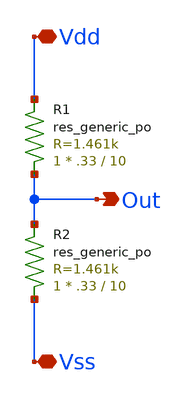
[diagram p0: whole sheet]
** sch_path: xschem/voltage_divider.sch
**.subckt voltage_divider Out Vdd Vss
*.opin Out
*.iopin Vdd
*.iopin Vss
XR1 Out Vdd sky130_fd_pr__res_generic_po W=.33 L=10 m=1
XR2 Vss Out sky130_fd_pr__res_generic_po W=.33 L=10 m=1
**.ends
.end
